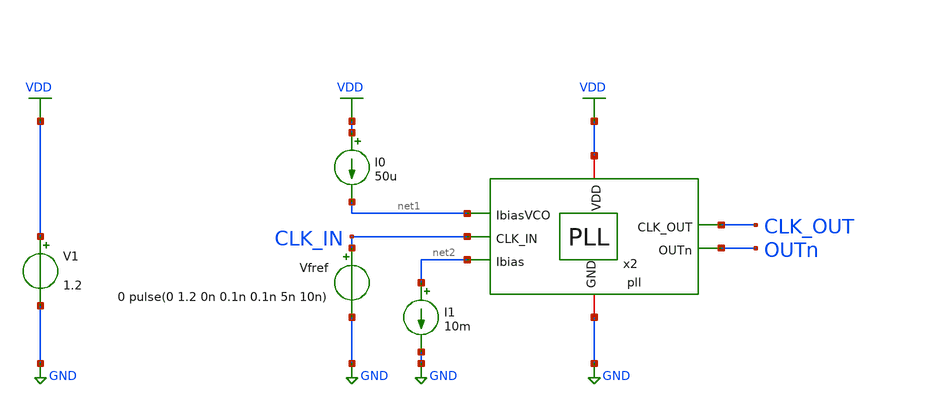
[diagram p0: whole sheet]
** sch_path: schematic/blocks/top-pll/top_pll_tb.sch
**.subckt top_pll_tb
V1 VDD GND 1.2
I0 VDD net1 50u
Vfref CLK_IN GND 0 pulse(0 1.2 0n 0.1n 0.1n 5n 10n)
I1 net2 GND 10m
x2 CLK_OUT CLK_IN net1 OUTn net2 VDD GND pll
**** begin user architecture code



*****************************************************
* PLL + DSM Frequency Divider Testbench
*****************************************************

.option temp = 27
.param VDD = 1.2

* ==============================
* Include Models
* ==============================

* Inductor / analog models
.include ./IHP_4nH_Inductor.spice

.control
  save x2.up x2.dn x2.vctrl x2.clk_in x2.clk_out x2.dsm_out clk_in clk_out outn
  *save v(sdata) v(sclk) v(rst) v(en) v(UP) v(DN) v(VCTRL) v(CLK_IN) v(DSM_OUT) v(CLK_OUT)
  * Simulation accuracy options
  .options maxstep=10p reltol=1e-4 abstol=1e-9

 * Run long enough for PLL lock
  tran 20p 1u uic
  remzerovec
  write pll_top.raw
.endc
* to generate following file copy stimuli.test
* to the simulation directory and run simulation -> Utile Stimuli Editor (GUI),
* and press 'Translate'
.include stimuli_test.cir






.lib cornerMOSlv.lib mos_tt
.lib cornerHBT.lib hbt_typ
.lib cornerRES.lib res_typ
.lib cornerCAP.lib cap_typ_stat
.include /foss/pdks/ihp-sg13g2/libs.ref/sg13g2_stdcell/spice/sg13g2_stdcell.spice
.global VDD GND


.param CP_N_L = 0.5u
.param CP_N_W = 10u
.param CP_P_M = 1
.param CP_P_L = 0.5u
.param CP_P_W = 30u
.param CP_N_M = 1
.param C_CP = 400p



**** end user architecture code
**.ends
.GLOBAL GND
.GLOBAL VDD
.end
